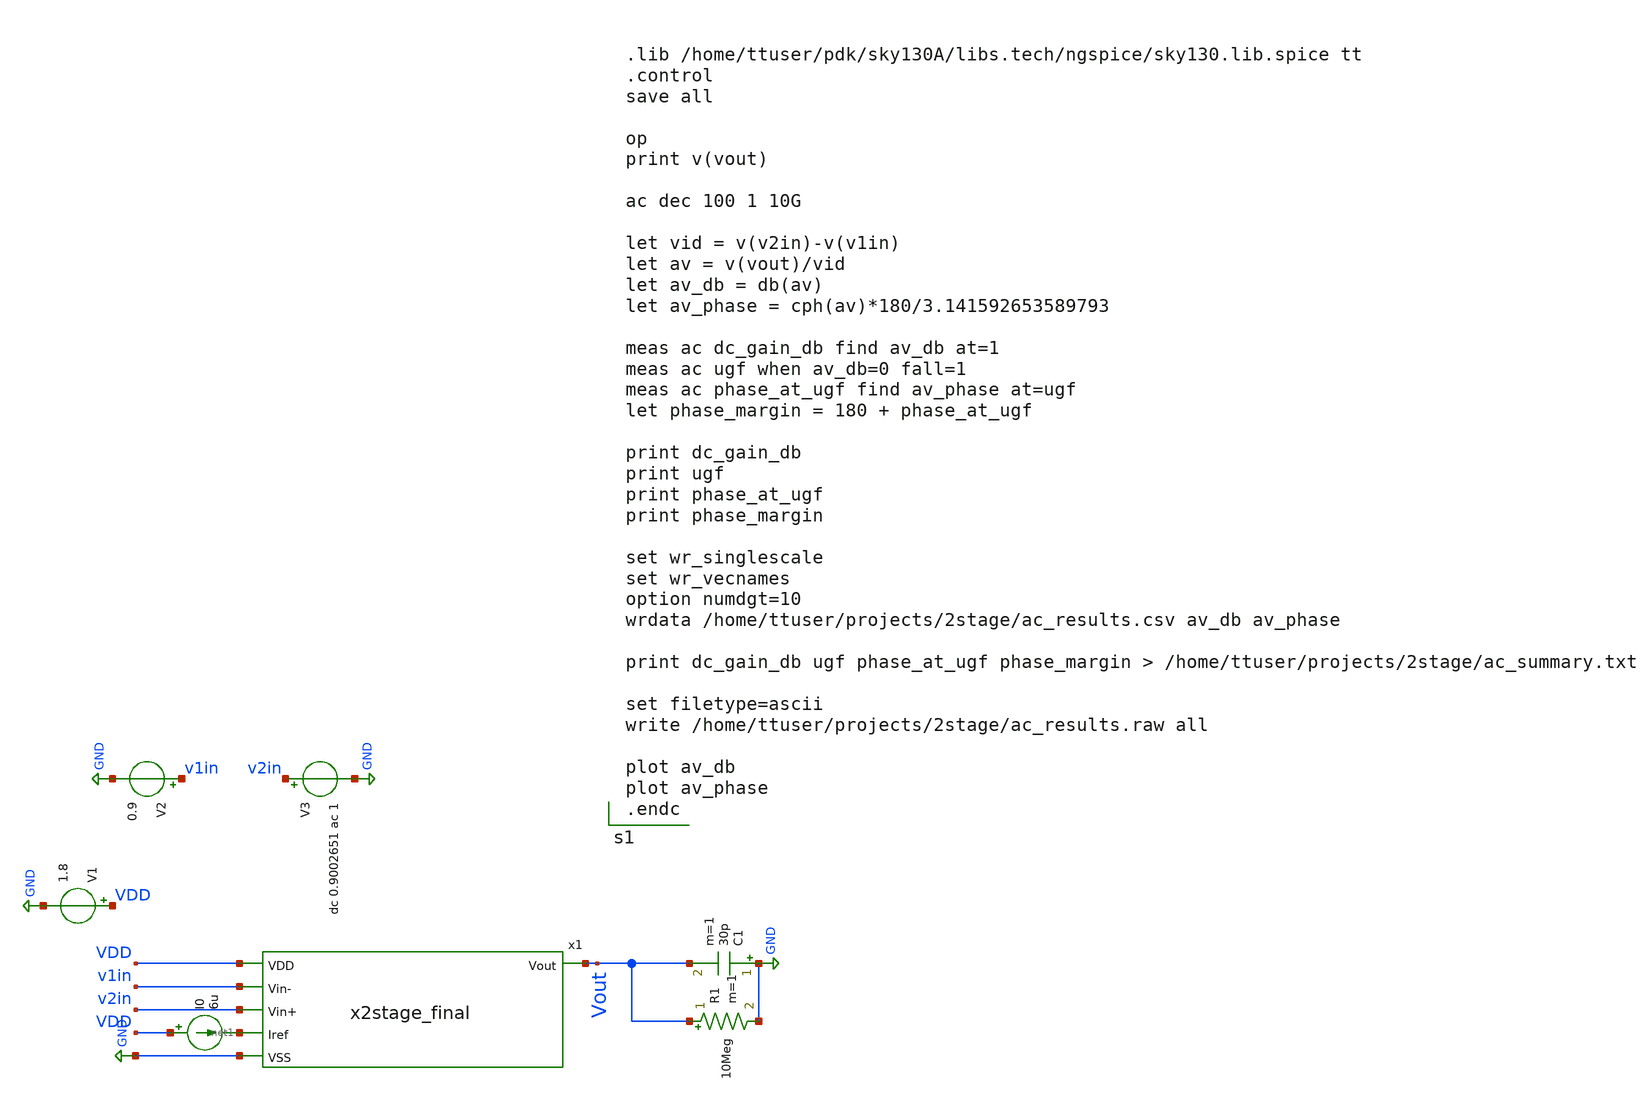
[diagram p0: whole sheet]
** sch_path: testbenches/postlayout/2stage_OL_pex.sch
**.subckt 2stage_OL_pex
x1 VDD Vout v1in v2in net1 GND x2stage_final
I0 VDD net1 6u
V1 VDD GND 1.8
V2 v1in GND 0.9
V3 v2in GND dc 0.9002651 ac 1
C1 GND Vout 30p m=1
R1 Vout GND 10Meg m=1
**** begin user architecture code


.lib /home/ttuser/pdk/sky130A/libs.tech/ngspice/sky130.lib.spice tt
.control
save all

op
print v(vout)

ac dec 100 1 10G

let vid = v(v2in)-v(v1in)
let av = v(vout)/vid
let av_db = db(av)
let av_phase = cph(av)*180/3.141592653589793

meas ac dc_gain_db find av_db at=1
meas ac ugf when av_db=0 fall=1
meas ac phase_at_ugf find av_phase at=ugf
let phase_margin = 180 + phase_at_ugf

print dc_gain_db
print ugf
print phase_at_ugf
print phase_margin

set wr_singlescale
set wr_vecnames
option numdgt=10
wrdata /home/ttuser/projects/2stage/ac_results.csv av_db av_phase

print dc_gain_db ugf phase_at_ugf phase_margin > /home/ttuser/projects/2stage/ac_summary.txt

set filetype=ascii
write /home/ttuser/projects/2stage/ac_results.raw all

plot av_db
plot av_phase
.endc


**** end user architecture code
**.ends

* expanding   symbol:  /home/ttuser/projects/xschem_test/x2stage_final.sym # of pins=6
** sym_path: schematic/diffpair.sym
.include /home/ttuser/projects/2stage/2stage_pex.spice
.GLOBAL GND
.end
